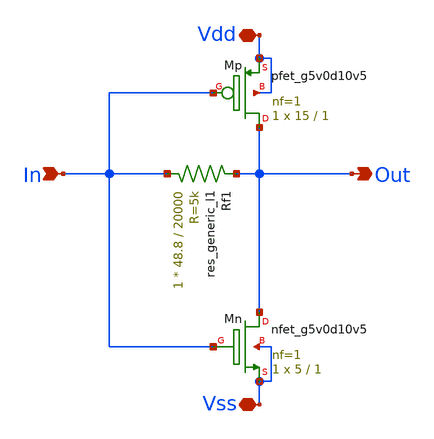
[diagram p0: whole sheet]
** sch_path: Vector-Matrix-Multiplicaction/xschem/TIA.sch
**.subckt TIA In Out Vdd Vss
*.ipin In
*.opin Out
*.iopin Vdd
*.iopin Vss
Rf1 In Out sky130_fd_pr__res_generic_l1 W=48.8 L=20000 m=1
XMp Out In Vdd Vdd sky130_fd_pr__pfet_g5v0d10v5 L=1 W=15 nf=1 ad='int((nf+1)/2) * W/nf * 0.29' as='int((nf+2)/2) * W/nf * 0.29'
+ pd='2*int((nf+1)/2) * (W/nf + 0.29)' ps='2*int((nf+2)/2) * (W/nf + 0.29)' nrd='0.29 / W' nrs='0.29 / W'
+ sa=0 sb=0 sd=0 mult=1 m=1
XMn Out In Vss Vss sky130_fd_pr__nfet_g5v0d10v5 L=1 W=5 nf=1 ad='int((nf+1)/2) * W/nf * 0.29' as='int((nf+2)/2) * W/nf * 0.29'
+ pd='2*int((nf+1)/2) * (W/nf + 0.29)' ps='2*int((nf+2)/2) * (W/nf + 0.29)' nrd='0.29 / W' nrs='0.29 / W'
+ sa=0 sb=0 sd=0 mult=1 m=1
**.ends
.end
